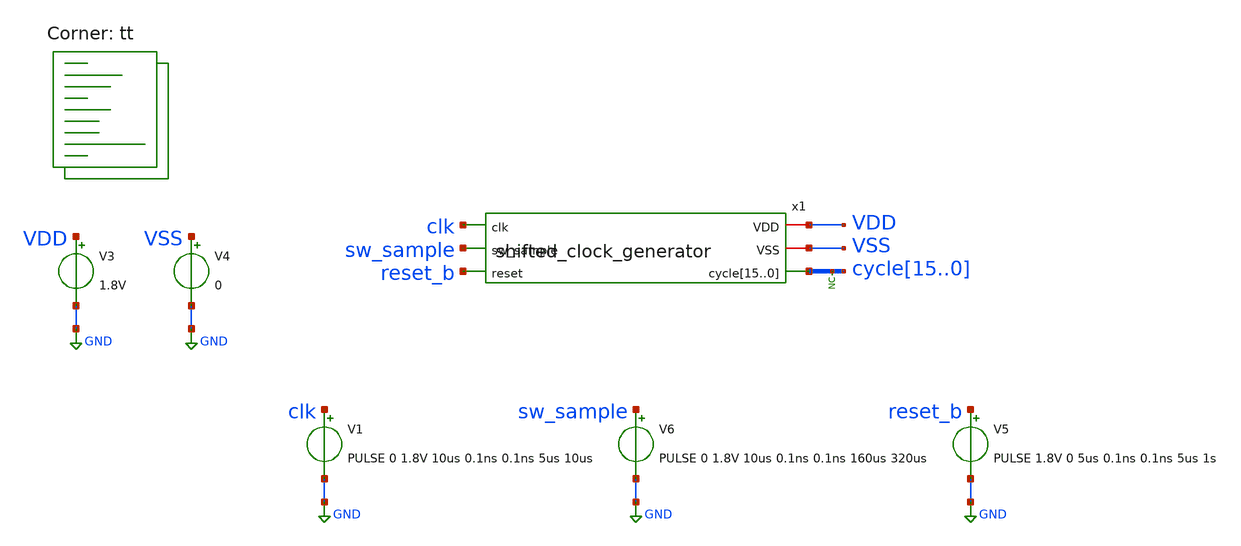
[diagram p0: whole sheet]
** sch_path: xschem/tests/shifted_clock_generator/shifted_clock_generator_test.sch
**.subckt shifted_clock_generator_test
V3 VDD GND 1.8V
V4 VSS GND 0
* noconn cycle[15..0]
V1 clk GND PULSE 0 1.8V 10us 0.1ns 0.1ns 5us 10us
V5 reset_b GND PULSE 1.8V 0 5us 0.1ns 0.1ns 5us 1s
x1 VDD clk sw_sample VSS reset_b cycle15 cycle14 cycle13 cycle12 cycle11 cycle10 cycle9 cycle8
+ cycle7 cycle6 cycle5 cycle4 cycle3 cycle2 cycle1 cycle0 shifted_clock_generator
V6 sw_sample GND PULSE 0 1.8V 10us 0.1ns 0.1ns 160us 320us
**** begin user architecture code
 *.lib $::SKYWATER_MODELS/sky130.lib.spice tt
.include $::SKYWATER_STDCELLS/sky130_fd_sc_hd.spice


.options acct list
.temp 25
*vvcc VDD 0 dc 1.8
*vvss VSS 0 0
.control
tran 0.1u 400u
*plot RST_PLS clk+2 Pulse+4
plot reset_b-6 clk-4 sw_sample-2 cycle0 cycle1+2 cycle2+4 cycle3+6 cycle4+8 cycle5+10 cycle6+12
+ cycle7+14 cycle8+16 cycle9+18 cycle10+20 cycle11+22 cycle12+24 cycle13+26 cycle14+28 cycle15+30

write shifted_clock_generator_test.raw
.endc


.lib $::SKYWATER_MODELS/sky130.lib.spice tt
**** end user architecture code
**.ends

* expanding   symbol:  src/shifted_clock_generator/shifted_clock_generator.sym # of pins=6
** sym_path: xschem/src/shifted_clock_generator/shifted_clock_generator.sym
** sch_path: xschem/src/shifted_clock_generator/shifted_clock_generator.sch
.subckt shifted_clock_generator VDD clk sw_sample VSS reset cycle15 cycle14 cycle13 cycle12 cycle11
+ cycle10 cycle9 cycle8 cycle7 cycle6 cycle5 cycle4 cycle3 cycle2 cycle1 cycle0
*.opin
*+ cycle15,cycle14,cycle13,cycle12,cycle11,cycle10,cycle9,cycle8,cycle7,cycle6,cycle5,cycle4,cycle3,cycle2,cycle1,cycle0
*.iopin VSS
*.iopin VDD
*.ipin clk
*.ipin reset
*.ipin sw_sample
x32 net16 net17 reset_b VSS VSS VDD VDD net4 sky130_fd_sc_hd__dfrtp_1
x1 net5 net4 reset_b VSS VSS VDD VDD net18 sky130_fd_sc_hd__dfrtp_1
x2 net6 net18 reset_b VSS VSS VDD VDD net19 sky130_fd_sc_hd__dfrtp_1
x3 net7 net19 reset_b VSS VSS VDD VDD net20 sky130_fd_sc_hd__dfrtp_1
x4 net8 net20 reset_b VSS VSS VDD VDD net21 sky130_fd_sc_hd__dfrtp_1
x5 net9 net21 reset_b VSS VSS VDD VDD net22 sky130_fd_sc_hd__dfrtp_1
x6 net10 net22 reset_b VSS VSS VDD VDD net23 sky130_fd_sc_hd__dfrtp_1
x7 net11 net23 reset_b VSS VSS VDD VDD net24 sky130_fd_sc_hd__dfrtp_1
x8 net12 net24 reset_b VSS VSS VDD VDD net25 sky130_fd_sc_hd__dfrtp_1
x9 net13 net25 reset_b VSS VSS VDD VDD net26 sky130_fd_sc_hd__dfrtp_1
x10 net14 net26 reset_b VSS VSS VDD VDD net27 sky130_fd_sc_hd__dfrtp_1
x11 net15 net27 reset_b VSS VSS VDD VDD net28 sky130_fd_sc_hd__dfrtp_1
x12 net3 net28 reset_b VSS VSS VDD VDD net29 sky130_fd_sc_hd__dfrtp_1
x13 net1 net29 reset_b VSS VSS VDD VDD net30 sky130_fd_sc_hd__dfrtp_1
x14 net2 net30 reset_b VSS VSS VDD VDD net31 sky130_fd_sc_hd__dfrtp_1
x31 net32 net33 reset_b VSS VSS VDD VDD net17 sky130_fd_sc_hd__dfrtp_1
x37 net35 VSS VSS VDD VDD reset_b sky130_fd_sc_hd__buf_16
x35 net34 reset VSS VSS VDD VDD net35 sky130_fd_sc_hd__and2_4
x15 net17 VSS VSS VDD VDD net46 sky130_fd_sc_hd__buf_1
x16 net44 VSS VSS VDD VDD net36 sky130_fd_sc_hd__buf_2
x20 net44 VSS VSS VDD VDD net37 sky130_fd_sc_hd__buf_2
x21 net44 VSS VSS VDD VDD net38 sky130_fd_sc_hd__buf_2
x22 net44 VSS VSS VDD VDD net39 sky130_fd_sc_hd__buf_2
x23 net45 VSS VSS VDD VDD net40 sky130_fd_sc_hd__buf_2
x24 net45 VSS VSS VDD VDD net41 sky130_fd_sc_hd__buf_2
x25 net45 VSS VSS VDD VDD net42 sky130_fd_sc_hd__buf_2
x26 net45 VSS VSS VDD VDD net43 sky130_fd_sc_hd__buf_2
x27 clk VSS VSS VDD VDD net44 sky130_fd_sc_hd__buf_4
x28 clk VSS VSS VDD VDD net45 sky130_fd_sc_hd__buf_4
x17 net36 VSS VSS VDD VDD net32 sky130_fd_sc_hd__buf_1
x18 net36 VSS VSS VDD VDD net16 sky130_fd_sc_hd__buf_1
x19 net37 VSS VSS VDD VDD net5 sky130_fd_sc_hd__buf_1
x29 net37 VSS VSS VDD VDD net6 sky130_fd_sc_hd__buf_1
x30 net38 VSS VSS VDD VDD net7 sky130_fd_sc_hd__buf_1
x33 net38 VSS VSS VDD VDD net8 sky130_fd_sc_hd__buf_1
x47 net39 VSS VSS VDD VDD net9 sky130_fd_sc_hd__buf_1
x48 net39 VSS VSS VDD VDD net10 sky130_fd_sc_hd__buf_1
x51 net40 VSS VSS VDD VDD net11 sky130_fd_sc_hd__buf_1
x52 net40 VSS VSS VDD VDD net12 sky130_fd_sc_hd__buf_1
x53 net41 VSS VSS VDD VDD net13 sky130_fd_sc_hd__buf_1
x54 net41 VSS VSS VDD VDD net14 sky130_fd_sc_hd__buf_1
x55 net42 VSS VSS VDD VDD net15 sky130_fd_sc_hd__buf_1
x56 net42 VSS VSS VDD VDD net3 sky130_fd_sc_hd__buf_1
x57 net43 VSS VSS VDD VDD net1 sky130_fd_sc_hd__buf_1
x58 net43 VSS VSS VDD VDD net2 sky130_fd_sc_hd__buf_1
x62 net4 VSS VSS VDD VDD net47 sky130_fd_sc_hd__buf_1
x66 net18 VSS VSS VDD VDD net48 sky130_fd_sc_hd__buf_1
x70 net19 VSS VSS VDD VDD net49 sky130_fd_sc_hd__buf_1
x34 sw_sample VSS VSS VDD VDD net34 sky130_fd_sc_hd__inv_1
x36 VDD VSS VSS VDD VDD net33 sky130_fd_sc_hd__buf_1
x38 net46 VSS VSS VDD VDD cycle0 sky130_fd_sc_hd__buf_4
x39 net47 VSS VSS VDD VDD cycle1 sky130_fd_sc_hd__buf_4
x40 net48 VSS VSS VDD VDD cycle2 sky130_fd_sc_hd__buf_4
x41 net49 VSS VSS VDD VDD cycle3 sky130_fd_sc_hd__buf_4
x42 net20 VSS VSS VDD VDD net50 sky130_fd_sc_hd__buf_1
x43 net21 VSS VSS VDD VDD net51 sky130_fd_sc_hd__buf_1
x44 net22 VSS VSS VDD VDD net52 sky130_fd_sc_hd__buf_1
x45 net23 VSS VSS VDD VDD net53 sky130_fd_sc_hd__buf_1
x46 net50 VSS VSS VDD VDD cycle4 sky130_fd_sc_hd__buf_4
x49 net51 VSS VSS VDD VDD cycle5 sky130_fd_sc_hd__buf_4
x50 net52 VSS VSS VDD VDD cycle6 sky130_fd_sc_hd__buf_4
x59 net53 VSS VSS VDD VDD cycle7 sky130_fd_sc_hd__buf_4
x60 net24 VSS VSS VDD VDD net54 sky130_fd_sc_hd__buf_1
x61 net25 VSS VSS VDD VDD net55 sky130_fd_sc_hd__buf_1
x63 net26 VSS VSS VDD VDD net56 sky130_fd_sc_hd__buf_1
x64 net27 VSS VSS VDD VDD net57 sky130_fd_sc_hd__buf_1
x65 net54 VSS VSS VDD VDD cycle8 sky130_fd_sc_hd__buf_4
x67 net55 VSS VSS VDD VDD cycle9 sky130_fd_sc_hd__buf_4
x68 net56 VSS VSS VDD VDD cycle10 sky130_fd_sc_hd__buf_4
x69 net57 VSS VSS VDD VDD cycle11 sky130_fd_sc_hd__buf_4
x71 net28 VSS VSS VDD VDD net58 sky130_fd_sc_hd__buf_1
x72 net29 VSS VSS VDD VDD net59 sky130_fd_sc_hd__buf_1
x73 net30 VSS VSS VDD VDD net60 sky130_fd_sc_hd__buf_1
x74 net31 VSS VSS VDD VDD net61 sky130_fd_sc_hd__buf_1
x75 net58 VSS VSS VDD VDD cycle12 sky130_fd_sc_hd__buf_4
x76 net59 VSS VSS VDD VDD cycle13 sky130_fd_sc_hd__buf_4
x77 net60 VSS VSS VDD VDD cycle14 sky130_fd_sc_hd__buf_4
x78 net61 VSS VSS VDD VDD cycle15 sky130_fd_sc_hd__buf_4
.ends

.GLOBAL GND
.end
